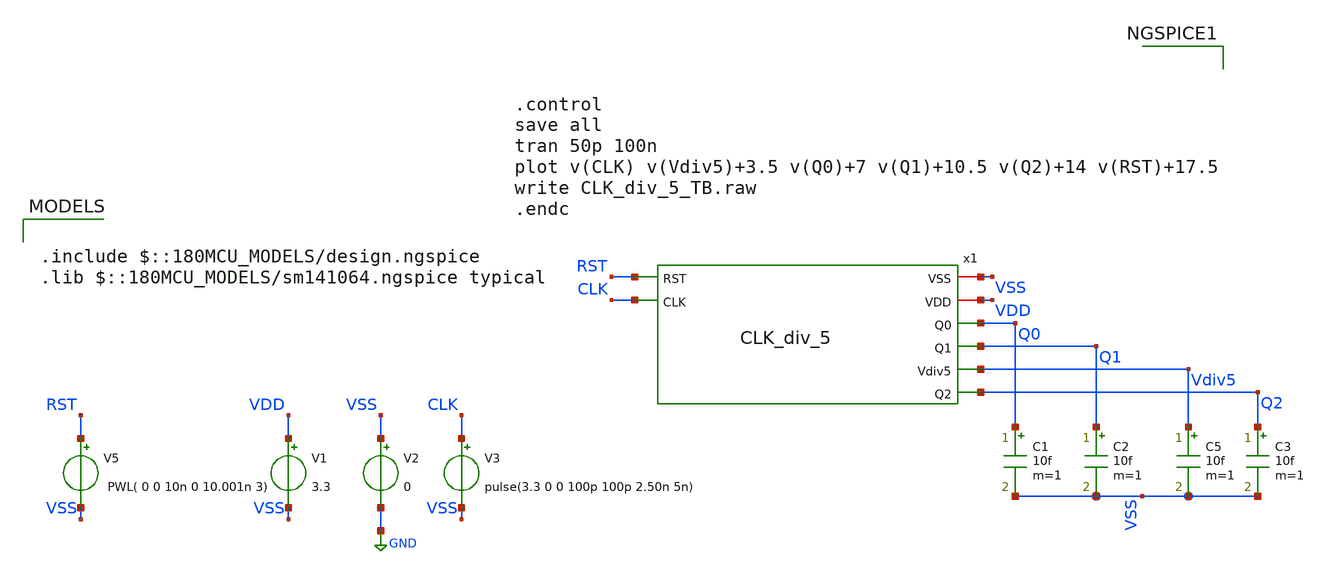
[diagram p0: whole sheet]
** sch_path: Clock_Generator_PAKISTAN_02/xschem/CLK_div_5_TB.sch
**.subckt CLK_div_5_TB
V1 VDD VSS 3.3
V2 VSS GND 0
V3 CLK VSS pulse(3.3 0 0 100p 100p 2.50n 5n)
C1 Q0 VSS 10f m=1
C2 Q1 VSS 10f m=1
C5 Vdiv5 VSS 10f m=1
V5 RST VSS PWL( 0 0 10n 0 10.001n 3)
x1 VSS VDD Q0 Q1 RST Vdiv5 Q2 CLK CLK_div_5
C3 Q2 VSS 10f m=1
**** begin user architecture code

.include $::180MCU_MODELS/design.ngspice
.lib $::180MCU_MODELS/sm141064.ngspice typical




.control
save all
tran 50p 100n
plot v(CLK) v(Vdiv5)+3.5 v(Q0)+7 v(Q1)+10.5 v(Q2)+14 v(RST)+17.5
write CLK_div_5_TB.raw
.endc


**** end user architecture code
**.ends
.GLOBAL GND
.end
